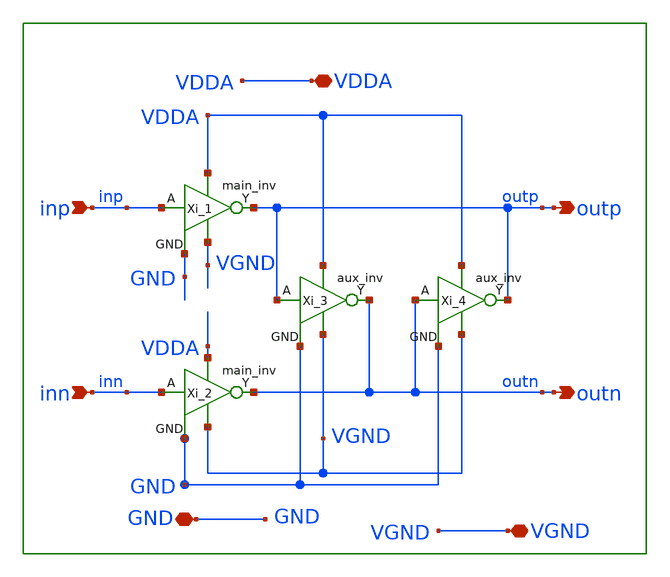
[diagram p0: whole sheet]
** sch_path: xschem/lib/cc_inv.sch
**.subckt cc_inv outp inn VGND outn inp VDDA GND
*.opin outp
*.ipin inn
*.iopin VGND
*.opin outn
*.ipin inp
*.iopin VDDA
*.iopin GND
Xi_1 inp outp VGND VDDA GND main_inv
Xi_2 inn outn VGND VDDA GND main_inv
Xi_3 VDDA VGND outn GND outp aux_inv
Xi_4 VDDA VGND outp GND outn aux_inv
**.ends

* expanding   symbol:  main_inv.sym # of pins=5
** sym_path: xschem/lib/main_inv.sym
** sch_path: xschem/lib/main_inv.sch
.subckt main_inv A Y VGND VDDA GND
*.iopin VDDA
*.iopin VGND
*.ipin A
*.opin Y
*.iopin GND
XM2 Y A VGND GND sky130_fd_pr__nfet_01v8 L=3.65 W=8 nf=2 ad='int((nf+1)/2) * W/nf * 0.29' as='int((nf+2)/2) * W/nf * 0.29'
+ pd='2*int((nf+1)/2) * (W/nf + 0.29)' ps='2*int((nf+2)/2) * (W/nf + 0.29)' nrd='0.29 / W' nrs='0.29 / W'
+ sa=0 sb=0 sd=0 mult=1 m=1
XM1 Y A VDDA VDDA sky130_fd_pr__pfet_01v8 L=3.65 W=10 nf=2 ad='int((nf+1)/2) * W/nf * 0.29' as='int((nf+2)/2) * W/nf * 0.29'
+ pd='2*int((nf+1)/2) * (W/nf + 0.29)' ps='2*int((nf+2)/2) * (W/nf + 0.29)' nrd='0.29 / W' nrs='0.29 / W'
+ sa=0 sb=0 sd=0 mult=1 m=1
.ends


* expanding   symbol:  aux_inv.sym # of pins=5
** sym_path: xschem/lib/aux_inv.sym
** sch_path: xschem/lib/aux_inv.sch
.subckt aux_inv VDDA VGND Y GND A
*.iopin VDDA
*.iopin VGND
*.ipin A
*.opin Y
*.iopin GND
XM3 Y A VGND GND sky130_fd_pr__nfet_01v8 L=3.65 W=4 nf=1 ad='int((nf+1)/2) * W/nf * 0.29' as='int((nf+2)/2) * W/nf * 0.29'
+ pd='2*int((nf+1)/2) * (W/nf + 0.29)' ps='2*int((nf+2)/2) * (W/nf + 0.29)' nrd='0.29 / W' nrs='0.29 / W'
+ sa=0 sb=0 sd=0 mult=1 m=1
XM2 Y A VDDA VDDA sky130_fd_pr__pfet_01v8 L=3.65 W=5 nf=1 ad='int((nf+1)/2) * W/nf * 0.29' as='int((nf+2)/2) * W/nf * 0.29'
+ pd='2*int((nf+1)/2) * (W/nf + 0.29)' ps='2*int((nf+2)/2) * (W/nf + 0.29)' nrd='0.29 / W' nrs='0.29 / W'
+ sa=0 sb=0 sd=0 mult=1 m=1
.ends

.end
